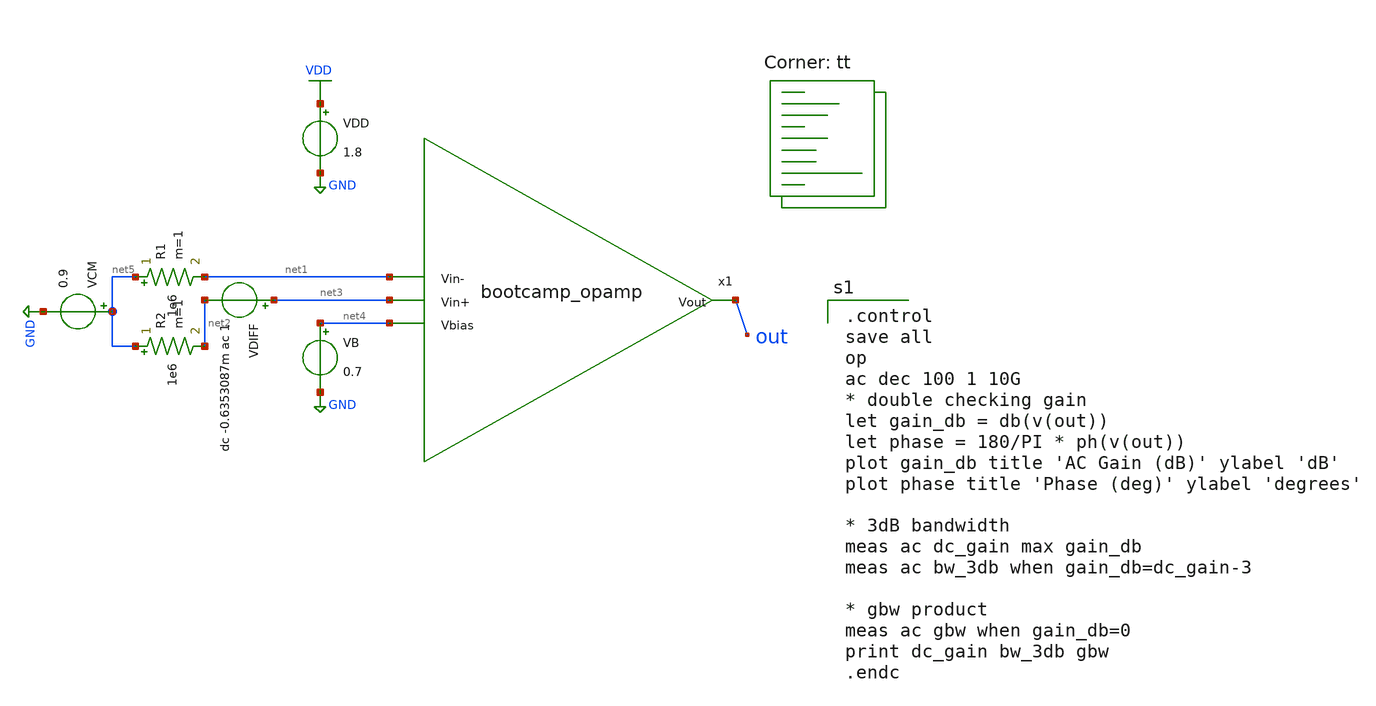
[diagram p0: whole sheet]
** sch_path: analog/schematics/tb_ac_analysis.sch
**.subckt tb_ac_analysis
x1 out net1 net3 net4 bootcamp_opamp
VDD VDD GND 1.8
VCM net5 GND 0.9
VB net4 GND 0.7
VDIFF net3 net2 dc -0.6353087m ac 1
R1 net5 net1 1e6 m=1
R2 net5 net2 1e6 m=1
**** begin user architecture code

.control
save all
op
ac dec 100 1 10G
* double checking gain
let gain_db = db(v(out))
let phase = 180/PI * ph(v(out))
plot gain_db title 'AC Gain (dB)' ylabel 'dB'
plot phase title 'Phase (deg)' ylabel 'degrees'

* 3dB bandwidth
meas ac dc_gain max gain_db
meas ac bw_3db when gain_db=dc_gain-3

* gbw product
meas ac gbw when gain_db=0
print dc_gain bw_3db gbw
.endc

.lib $::SKYWATER_MODELS/sky130.lib.spice tt
**** end user architecture code
**.ends
.GLOBAL GND
.GLOBAL VDD
.end
